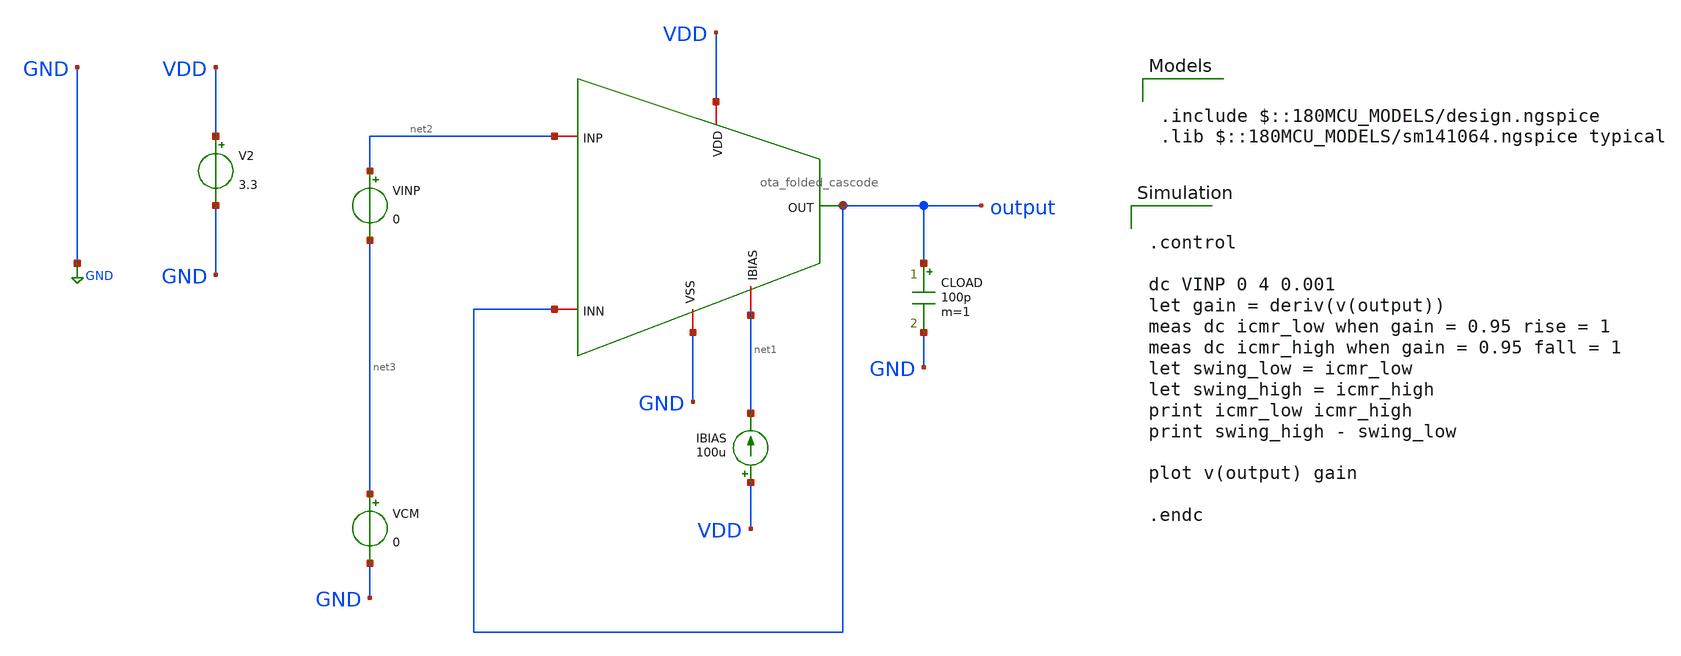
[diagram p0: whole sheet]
** sch_path: designs/libs/core_amps/ota_folded_cascode/dc_unity_tb.sch
**.subckt dc_unity_tb
IBIAS VDD net1 100u
V2 VDD GND 3.3
CLOAD output GND 100p m=1
VINP net2 net3 0
VCM net3 GND 0
x1 VDD GND output net2 output net1 ota_folded_cascode
**** begin user architecture code

.include $::180MCU_MODELS/design.ngspice
.lib $::180MCU_MODELS/sm141064.ngspice typical



.control

dc VINP 0 4 0.001
let gain = deriv(v(output))
meas dc icmr_low when gain = 0.95 rise = 1
meas dc icmr_high when gain = 0.95 fall = 1
let swing_low = icmr_low
let swing_high = icmr_high
print icmr_low icmr_high
print swing_high - swing_low

plot v(output) gain

.endc


**** end user architecture code
**.ends
.GLOBAL GND
.end
